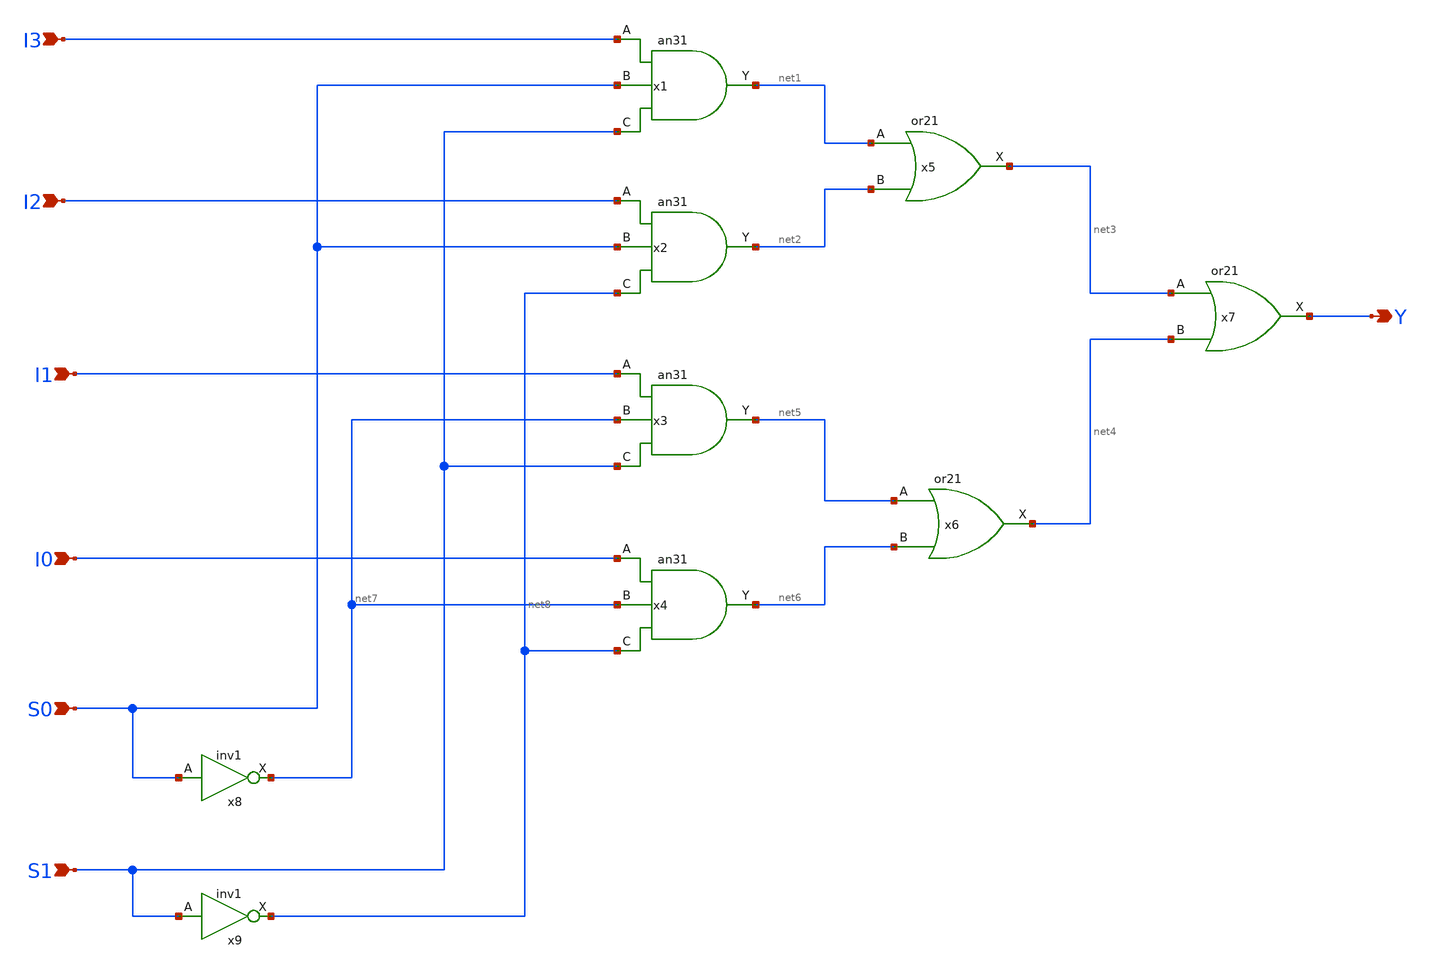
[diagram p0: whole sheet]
** sch_path: member_project/ishi-kai/4ch_mux.sch
**.subckt 4ch_mux I3 I2 I1 I0 S0 S1 Y
*.ipin I3
*.ipin I2
*.ipin I1
*.ipin I0
*.ipin S0
*.ipin S1
*.opin Y
x1 I3 S0 S1 VDD GND net1 an31
x2 I2 S0 net8 VDD GND net2 an31
x3 I1 net7 S1 VDD GND net5 an31
x4 I0 net7 net8 VDD GND net6 an31
x5 net1 net2 VDD GND net3 or21
x6 net5 net6 VDD GND net4 or21
x7 net3 net4 VDD GND Y or21
x8 S0 VDD GND net7 inv1
x9 S1 VDD GND net8 inv1
**.ends
.end
